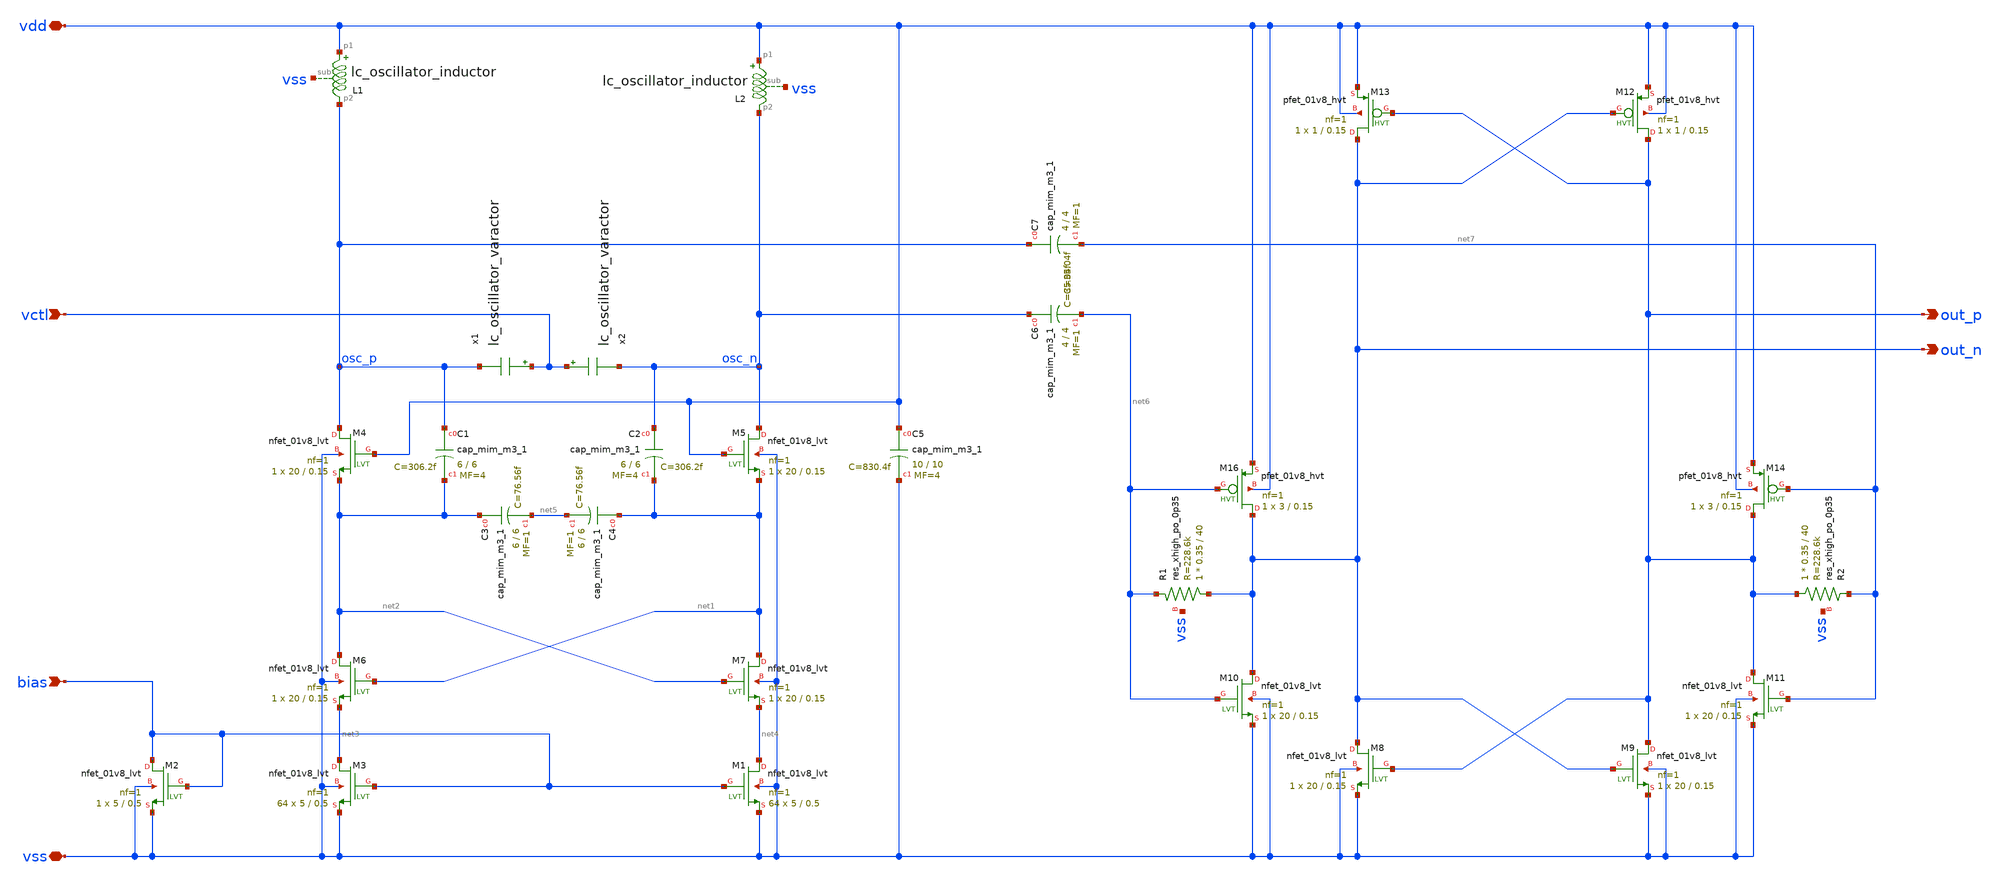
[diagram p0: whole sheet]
** sch_path: design/lc_oscillator/lc_oscillator.sch
**.subckt lc_oscillator vctl vss bias vdd out_p out_n
*.ipin vctl
*.iopin vss
*.ipin bias
*.iopin vdd
*.opin out_p
*.opin out_n
XM2 bias bias vss vss sky130_fd_pr__nfet_01v8_lvt L=0.5 W=5 nf=1 ad='int((nf+1)/2) * W/nf * 0.29' as='int((nf+2)/2) * W/nf * 0.29'
+ pd='2*int((nf+1)/2) * (W/nf + 0.29)' ps='2*int((nf+2)/2) * (W/nf + 0.29)' nrd='0.29 / W' nrs='0.29 / W'
+ sa=0 sb=0 sd=0 mult=1 m=1
XM1 net4 bias vss vss sky130_fd_pr__nfet_01v8_lvt L=0.5 W=5 nf=1 ad='int((nf+1)/2) * W/nf * 0.29' as='int((nf+2)/2) * W/nf * 0.29'
+ pd='2*int((nf+1)/2) * (W/nf + 0.29)' ps='2*int((nf+2)/2) * (W/nf + 0.29)' nrd='0.29 / W' nrs='0.29 / W'
+ sa=0 sb=0 sd=0 mult=64 m=64
XM3 net3 bias vss vss sky130_fd_pr__nfet_01v8_lvt L=0.5 W=5 nf=1 ad='int((nf+1)/2) * W/nf * 0.29' as='int((nf+2)/2) * W/nf * 0.29'
+ pd='2*int((nf+1)/2) * (W/nf + 0.29)' ps='2*int((nf+2)/2) * (W/nf + 0.29)' nrd='0.29 / W' nrs='0.29 / W'
+ sa=0 sb=0 sd=0 mult=64 m=64
XC1 osc_p net2 sky130_fd_pr__cap_mim_m3_1 W=6 L=6 MF=4 m=4
XC2 osc_n net1 sky130_fd_pr__cap_mim_m3_1 W=6 L=6 MF=4 m=4
XC3 net2 net5 sky130_fd_pr__cap_mim_m3_1 W=6 L=6 MF=1 m=1
XC4 net1 net5 sky130_fd_pr__cap_mim_m3_1 W=6 L=6 MF=1 m=1
XM4 osc_p vdd net2 vss sky130_fd_pr__nfet_01v8_lvt L=0.15 W=20 nf=1 ad='int((nf+1)/2) * W/nf * 0.29'
+ as='int((nf+2)/2) * W/nf * 0.29' pd='2*int((nf+1)/2) * (W/nf + 0.29)' ps='2*int((nf+2)/2) * (W/nf + 0.29)'
+ nrd='0.29 / W' nrs='0.29 / W' sa=0 sb=0 sd=0 mult=1 m=1
XM5 osc_n vdd net1 vss sky130_fd_pr__nfet_01v8_lvt L=0.15 W=20 nf=1 ad='int((nf+1)/2) * W/nf * 0.29'
+ as='int((nf+2)/2) * W/nf * 0.29' pd='2*int((nf+1)/2) * (W/nf + 0.29)' ps='2*int((nf+2)/2) * (W/nf + 0.29)'
+ nrd='0.29 / W' nrs='0.29 / W' sa=0 sb=0 sd=0 mult=1 m=1
L1 vdd osc_p vss lc_oscillator_inductor
L2 vdd osc_n vss lc_oscillator_inductor
XM6 net2 net1 net3 vss sky130_fd_pr__nfet_01v8_lvt L=0.15 W=20 nf=1 ad='int((nf+1)/2) * W/nf * 0.29'
+ as='int((nf+2)/2) * W/nf * 0.29' pd='2*int((nf+1)/2) * (W/nf + 0.29)' ps='2*int((nf+2)/2) * (W/nf + 0.29)'
+ nrd='0.29 / W' nrs='0.29 / W' sa=0 sb=0 sd=0 mult=1 m=1
XM7 net1 net2 net4 vss sky130_fd_pr__nfet_01v8_lvt L=0.15 W=20 nf=1 ad='int((nf+1)/2) * W/nf * 0.29'
+ as='int((nf+2)/2) * W/nf * 0.29' pd='2*int((nf+1)/2) * (W/nf + 0.29)' ps='2*int((nf+2)/2) * (W/nf + 0.29)'
+ nrd='0.29 / W' nrs='0.29 / W' sa=0 sb=0 sd=0 mult=1 m=1
XC5 vdd vss sky130_fd_pr__cap_mim_m3_1 W=10 L=10 MF=4 m=4
x1 vctl osc_p lc_oscillator_varactor
x2 vctl osc_n lc_oscillator_varactor
XM8 out_n out_p vss vss sky130_fd_pr__nfet_01v8_lvt L=0.15 W=20 nf=1 ad='int((nf+1)/2) * W/nf * 0.29'
+ as='int((nf+2)/2) * W/nf * 0.29' pd='2*int((nf+1)/2) * (W/nf + 0.29)' ps='2*int((nf+2)/2) * (W/nf + 0.29)'
+ nrd='0.29 / W' nrs='0.29 / W' sa=0 sb=0 sd=0 mult=1 m=1
XM9 out_p out_n vss vss sky130_fd_pr__nfet_01v8_lvt L=0.15 W=20 nf=1 ad='int((nf+1)/2) * W/nf * 0.29'
+ as='int((nf+2)/2) * W/nf * 0.29' pd='2*int((nf+1)/2) * (W/nf + 0.29)' ps='2*int((nf+2)/2) * (W/nf + 0.29)'
+ nrd='0.29 / W' nrs='0.29 / W' sa=0 sb=0 sd=0 mult=1 m=1
XM10 out_n net6 vss vss sky130_fd_pr__nfet_01v8_lvt L=0.15 W=20 nf=1 ad='int((nf+1)/2) * W/nf * 0.29'
+ as='int((nf+2)/2) * W/nf * 0.29' pd='2*int((nf+1)/2) * (W/nf + 0.29)' ps='2*int((nf+2)/2) * (W/nf + 0.29)'
+ nrd='0.29 / W' nrs='0.29 / W' sa=0 sb=0 sd=0 mult=1 m=1
XM11 out_p net7 vss vss sky130_fd_pr__nfet_01v8_lvt L=0.15 W=20 nf=1 ad='int((nf+1)/2) * W/nf * 0.29'
+ as='int((nf+2)/2) * W/nf * 0.29' pd='2*int((nf+1)/2) * (W/nf + 0.29)' ps='2*int((nf+2)/2) * (W/nf + 0.29)'
+ nrd='0.29 / W' nrs='0.29 / W' sa=0 sb=0 sd=0 mult=1 m=1
XR1 out_n net6 vss sky130_fd_pr__res_xhigh_po_0p35 L=40 mult=1 m=1
XR2 out_p net7 vss sky130_fd_pr__res_xhigh_po_0p35 L=40 mult=1 m=1
XC6 osc_n net6 sky130_fd_pr__cap_mim_m3_1 W=4 L=4 MF=1 m=1
XC7 osc_p net7 sky130_fd_pr__cap_mim_m3_1 W=4 L=4 MF=1 m=1
XM16 out_n net6 vdd vdd sky130_fd_pr__pfet_01v8_hvt L=0.15 W=3 nf=1 ad='int((nf+1)/2) * W/nf * 0.29'
+ as='int((nf+2)/2) * W/nf * 0.29' pd='2*int((nf+1)/2) * (W/nf + 0.29)' ps='2*int((nf+2)/2) * (W/nf + 0.29)'
+ nrd='0.29 / W' nrs='0.29 / W' sa=0 sb=0 sd=0 mult=1 m=1
XM14 out_p net7 vdd vdd sky130_fd_pr__pfet_01v8_hvt L=0.15 W=3 nf=1 ad='int((nf+1)/2) * W/nf * 0.29'
+ as='int((nf+2)/2) * W/nf * 0.29' pd='2*int((nf+1)/2) * (W/nf + 0.29)' ps='2*int((nf+2)/2) * (W/nf + 0.29)'
+ nrd='0.29 / W' nrs='0.29 / W' sa=0 sb=0 sd=0 mult=1 m=1
XM12 out_p out_n vdd vdd sky130_fd_pr__pfet_01v8_hvt L=0.15 W=1 nf=1 ad='int((nf+1)/2) * W/nf * 0.29'
+ as='int((nf+2)/2) * W/nf * 0.29' pd='2*int((nf+1)/2) * (W/nf + 0.29)' ps='2*int((nf+2)/2) * (W/nf + 0.29)'
+ nrd='0.29 / W' nrs='0.29 / W' sa=0 sb=0 sd=0 mult=1 m=1
XM13 out_n out_p vdd vdd sky130_fd_pr__pfet_01v8_hvt L=0.15 W=1 nf=1 ad='int((nf+1)/2) * W/nf * 0.29'
+ as='int((nf+2)/2) * W/nf * 0.29' pd='2*int((nf+1)/2) * (W/nf + 0.29)' ps='2*int((nf+2)/2) * (W/nf + 0.29)'
+ nrd='0.29 / W' nrs='0.29 / W' sa=0 sb=0 sd=0 mult=1 m=1
**.ends

* expanding   symbol:  lc_oscillator_inductor/lc_oscillator_inductor.sym # of pins=3
** sym_path: design/lc_oscillator_inductor/lc_oscillator_inductor.sym
** sch_path: design/lc_oscillator_inductor/lc_oscillator_inductor.sch
.subckt lc_oscillator_inductor p1 p2 sub
*.iopin p2
*.iopin p1
*.iopin sub
L1 net1 p1 1.028n m=1
C1 p1 net2 62.02f m=1
R1 net2 sub 16.03 m=1
C2 p1 p2 0.1f m=1
C3 p2 net3 62.31f m=1
R2 net3 sub 15.88 m=1
R3 p2 net1 3.6825 m=1
.ends


* expanding   symbol:  lc_oscillator_varactor/lc_oscillator_varactor.sym # of pins=2
** sym_path: design/lc_oscillator_varactor/lc_oscillator_varactor.sym
** sch_path: design/lc_oscillator_varactor/lc_oscillator_varactor.sch
.subckt lc_oscillator_varactor p m
*.iopin p
*.iopin m
XMvaractor p m p p sky130_fd_pr__nfet_01v8 L=4 W=4 nf=3 ad='int((nf+1)/2) * W/nf * 0.29' as='int((nf+2)/2) * W/nf * 0.29'
+ pd='2*int((nf+1)/2) * (W/nf + 0.29)' ps='2*int((nf+2)/2) * (W/nf + 0.29)' nrd='0.29 / W' nrs='0.29 / W'
+ sa=0 sb=0 sd=0 mult=1 m=1
.ends

.end
